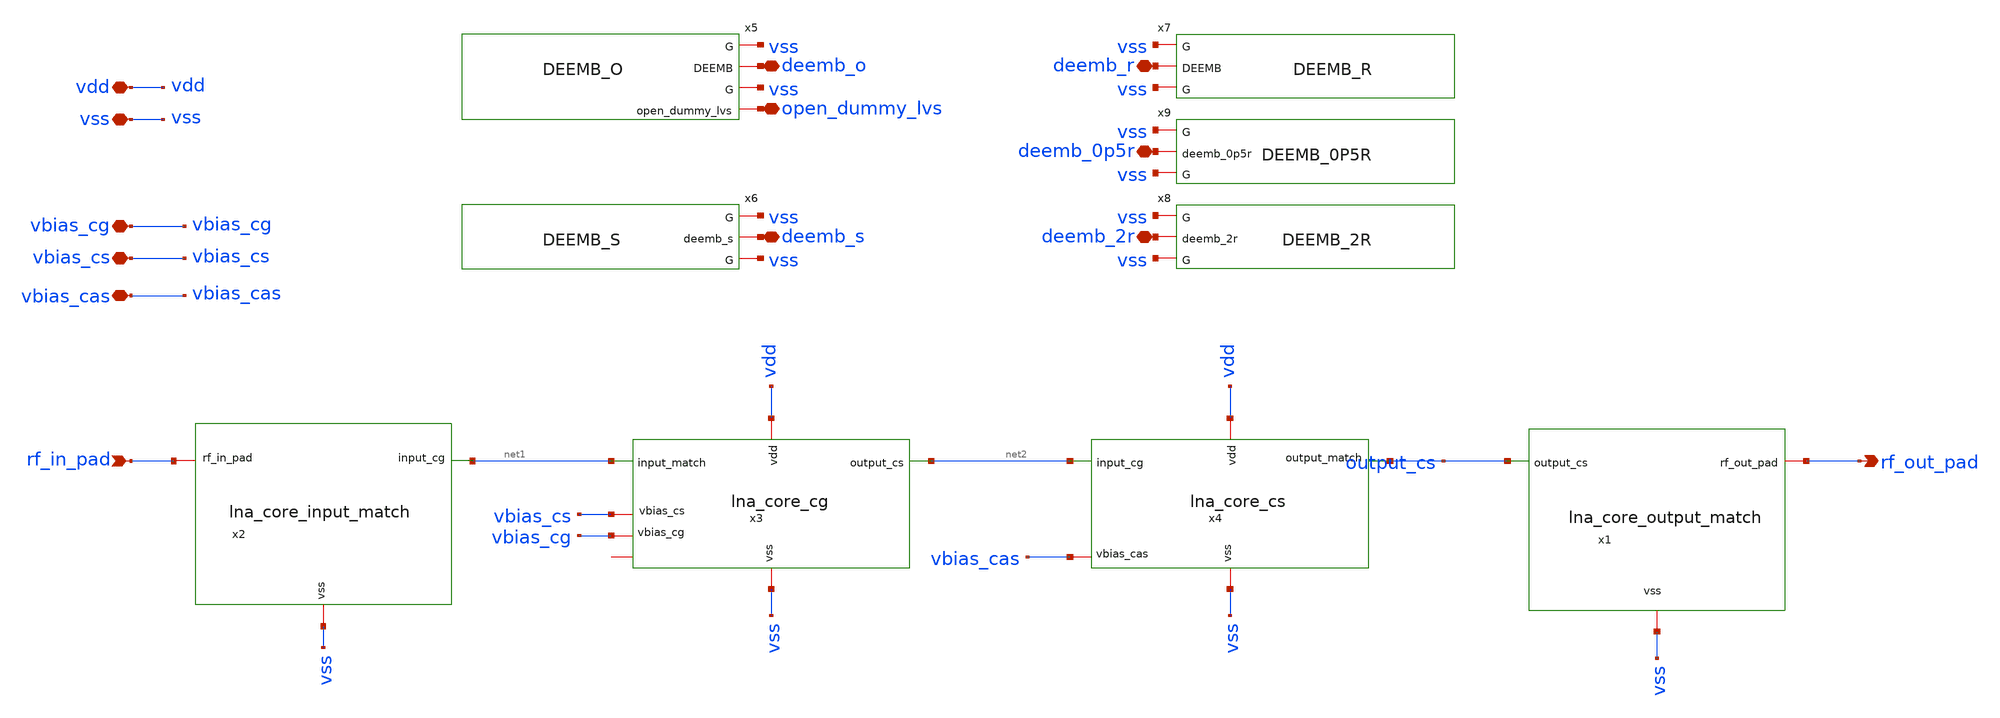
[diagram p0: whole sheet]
** sch_path: xschem/lna_core_parts.sch
**.subckt lna_core_parts rf_in_pad vbias_cg vbias_cs rf_out_pad vdd vss vbias_cas deemb_o deemb_s
*+ deemb_2r deemb_0p5r deemb_r open_dummy_lvs
*.ipin rf_in_pad
*.iopin vbias_cg
*.iopin vbias_cs
*.opin rf_out_pad
*.iopin vdd
*.iopin vss
*.iopin vbias_cas
*.iopin deemb_o
*.iopin deemb_s
*.iopin deemb_2r
*.iopin deemb_0p5r
*.iopin deemb_r
*.iopin open_dummy_lvs
x1 output_cs rf_out_pad vss lna_core_output_match
x2 vss net1 rf_in_pad lna_core_input_match
x3 vbias_cs vdd vss vbias_cg net2 net1 lna_core_cg
x4 output_cs vbias_cas net2 vdd vss lna_core_cs
x5 vss deemb_o open_dummy_lvs DEEMB_O
x6 vss deemb_s DEEMB_S
x7 vss deemb_r DEEMB_R
x8 vss deemb_2r DEEMB_2R
x9 vss deemb_0p5r DEEMB_0P5R
**** begin user architecture code

* LVS-only inductor model selection -- every coil in this hierarchy becomes
* a PDK metal resistor device instead of an inductor, so the official
* gf180mcu.lvs engine has something comparable to match against the
* layout's resistor-marker geometry (see xschem/*_model.lib for the other
* ideal/rl/snp2le simulation variants, untouched by this selection).
.lib $::env(PWD)/LEQ_model.lib lvsrm
.lib $::env(PWD)/L1_model.lib lvsrm
.lib $::env(PWD)/LSHUNT_OUT_model.lib lvsrm
.lib $::env(PWD)/LD2_model.lib lvsrm
.lib $::env(PWD)/LD4_model.lib lvsrm

**** end user architecture code
**.ends
.end
